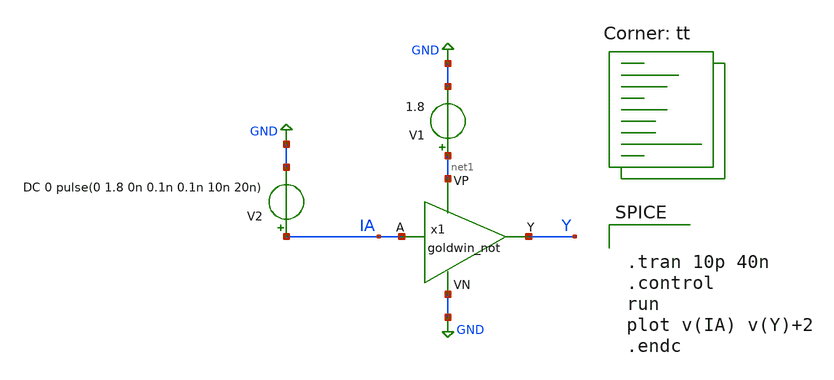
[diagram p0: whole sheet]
** sch_path: APIC-UTS/schematic/goldwin_not_v2/tb_goldwin_not_v2.sch
**.subckt tb_goldwin_not_v2
V1 net1 GND 1.8
V2 IA GND DC 0 pulse(0 1.8 0n 0.1n 0.1n 10n 20n)
x1 IA Y net1 GND goldwin_not
**** begin user architecture code


.tran 10p 40n
.control
run
plot v(IA) v(Y)+2
.endc


.lib $::SKYWATER_MODELS/sky130.lib.spice tt
**** end user architecture code
**.ends

* expanding   symbol:  goldwin_not.sym # of pins=4
** sym_path: APIC-UTS/schematic/goldwin_not/goldwin_not.sym
** sch_path: APIC-UTS/schematic/goldwin_not/goldwin_not.sch
.subckt goldwin_not A Y VP VN
*.ipin A
*.ipin VP
*.ipin VN
*.opin Y
XM1 Y A VN VN sky130_fd_pr__nfet_01v8 L=0.15 W=1 nf=1 ad='int((nf+1)/2) * W/nf * 0.29' as='int((nf+2)/2) * W/nf * 0.29'
+ pd='2*int((nf+1)/2) * (W/nf + 0.29)' ps='2*int((nf+2)/2) * (W/nf + 0.29)' nrd='0.29 / W' nrs='0.29 / W'
+ sa=0 sb=0 sd=0 mult=1 m=1
XM2 Y A VP VP sky130_fd_pr__pfet_01v8 L=0.15 W=3 nf=1 ad='int((nf+1)/2) * W/nf * 0.29' as='int((nf+2)/2) * W/nf * 0.29'
+ pd='2*int((nf+1)/2) * (W/nf + 0.29)' ps='2*int((nf+2)/2) * (W/nf + 0.29)' nrd='0.29 / W' nrs='0.29 / W'
+ sa=0 sb=0 sd=0 mult=1 m=1
.ends

.GLOBAL GND
.end
